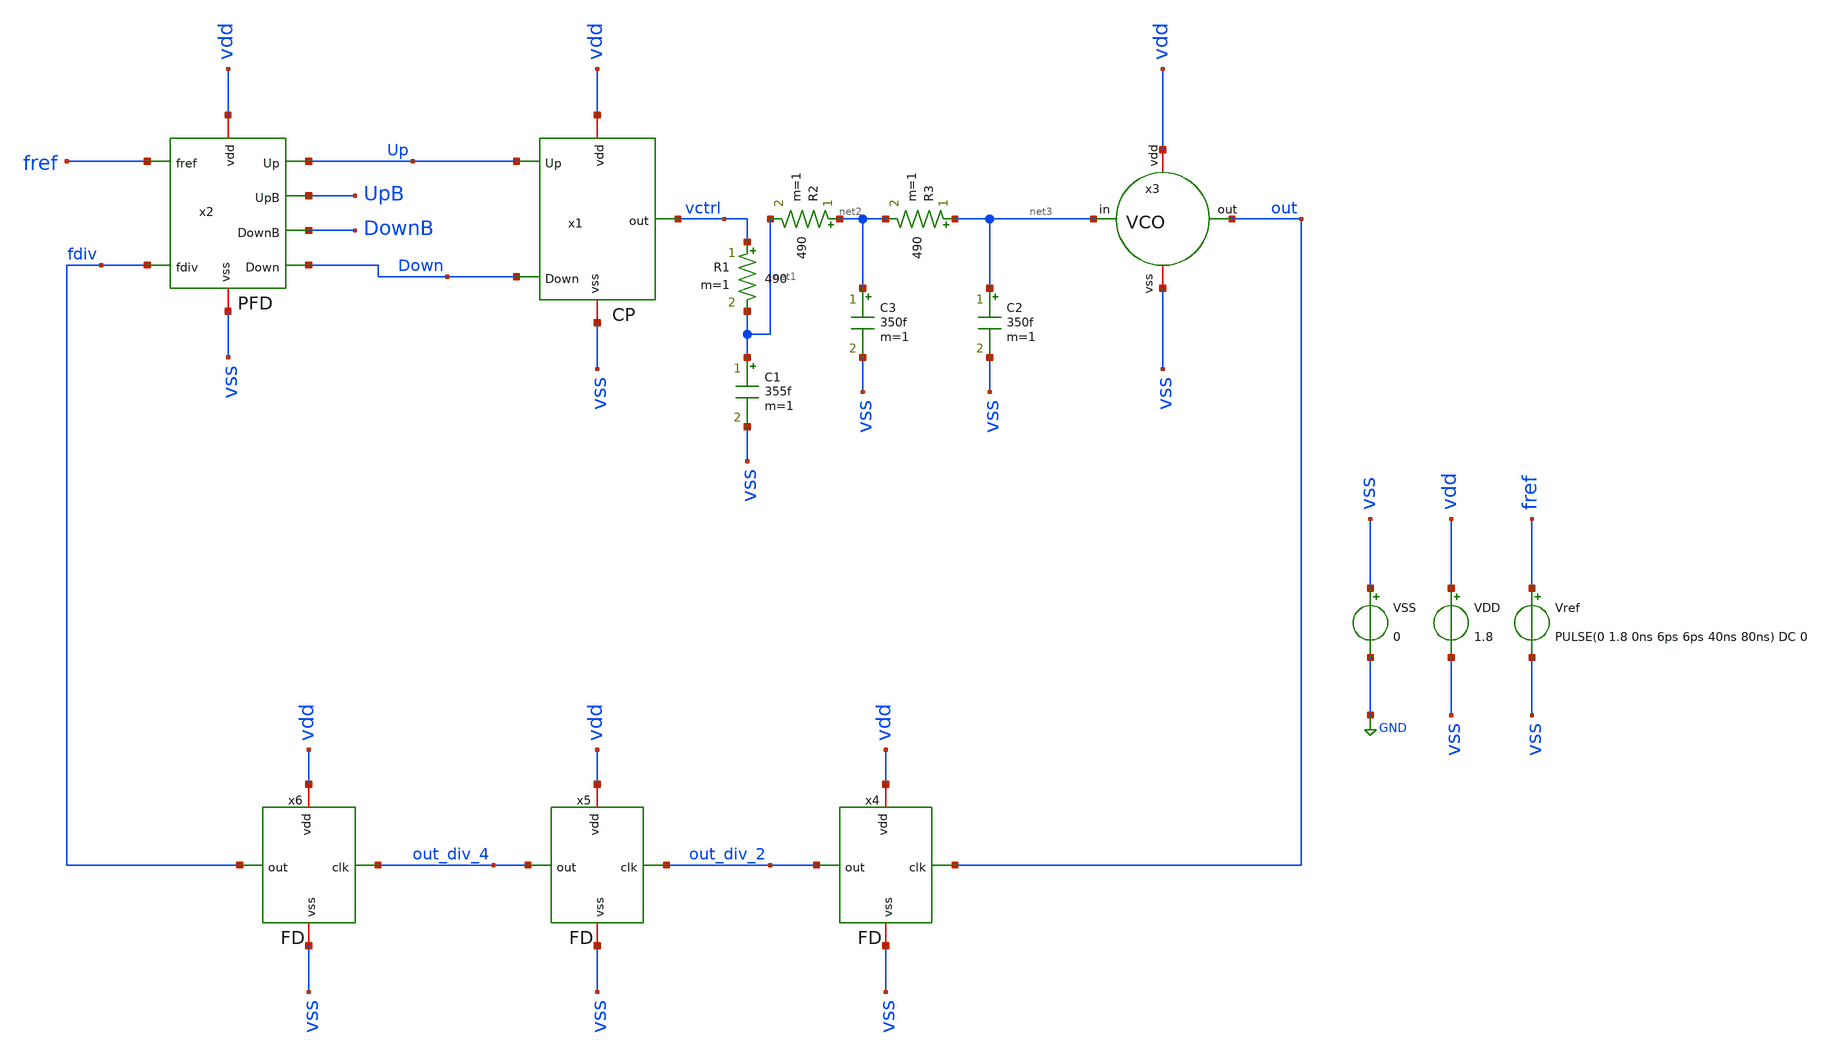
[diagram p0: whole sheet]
** sch_path: sch/PLL_caravel/PLL.sch
**.subckt PLL
x1 vdd Down vctrl Up vss CP
x2 vdd fref Up UpB DownB fdiv Down vss PFD
x3 vdd out net3 vss VCO
x4 out out_div_2 vdd vss FD
C1 net1 vss 355f m=1
R1 vctrl net1 490 m=1
R2 net2 net1 490 m=1
C3 net2 vss 350f m=1
R3 net3 net2 490 m=1
C2 net3 vss 350f m=1
x5 out_div_2 out_div_4 vdd vss FD
x6 out_div_4 fdiv vdd vss FD
VSS vss GND 0
VDD vdd vss 1.8
Vref fref vss PULSE(0 1.8 0ns 6ps 6ps 40ns 80ns) DC 0
**** begin user architecture code



* Parameters
.options TEMPS = 27.0

* Models
.lib ~/skywater/skywater-pdk/libraries/sky130_fd_pr_ngspice/latest/models/corners/sky130.lib TT

* Data to save
.save all

* Simulation
.ic v(vctrl) = 0
.ic v(out_div_2) = 0
.ic v(out_div_4) = 1.8
.ic v(fdiv) = 0
.control
	tran 0.1ns 50us
	plot v(fref)+18 v(fdiv)+18 v(out_div_4)+15 v(out_div_2)+12 v(out)+9 v(up)+6 v(down)+3 v(vctrl)
.endc

.end


**** end user architecture code
**.ends

* expanding   symbol:  PLL_caravel/CP.sym # of pins=5
** sym_path: sch/PLL_caravel/CP.sym
** sch_path: sch/PLL_caravel/CP.sch
.subckt CP vdd Down out Up vss
*.iopin vdd
*.ipin Down
*.opin out
*.iopin vss
*.ipin Up
XM1 outP net1 vdd vdd sky130_fd_pr__pfet_01v8 L=0.15 W=5.4 nf=1 ad='int((nf+1)/2) * W/nf * 0.29' as='int((nf+2)/2) * W/nf * 0.29'
+ pd='2*int((nf+1)/2) * (W/nf + 0.29)' ps='2*int((nf+2)/2) * (W/nf + 0.29)' nrd='0.29 / W' nrs='0.29 / W'
+ sa=0 sb=0 sd=0 mult=1 m=1
XM2 out Up outN vss sky130_fd_pr__nfet_01v8 L=0.15 W=0.42 nf=1 ad='int((nf+1)/2) * W/nf * 0.29' as='int((nf+2)/2) * W/nf * 0.29'
+ pd='2*int((nf+1)/2) * (W/nf + 0.29)' ps='2*int((nf+2)/2) * (W/nf + 0.29)' nrd='0.29 / W' nrs='0.29 / W'
+ sa=0 sb=0 sd=0 mult=1 m=1
XM3 net1 net1 vdd vdd sky130_fd_pr__pfet_01v8 L=0.15 W=0.42 nf=1 ad='int((nf+1)/2) * W/nf * 0.29' as='int((nf+2)/2) * W/nf * 0.29'
+ pd='2*int((nf+1)/2) * (W/nf + 0.29)' ps='2*int((nf+2)/2) * (W/nf + 0.29)' nrd='0.29 / W' nrs='0.29 / W'
+ sa=0 sb=0 sd=0 mult=1 m=1
XM4 out DownB outP vdd sky130_fd_pr__pfet_01v8 L=0.15 W=0.42 nf=1 ad='int((nf+1)/2) * W/nf * 0.29' as='int((nf+2)/2) * W/nf * 0.29'
+ pd='2*int((nf+1)/2) * (W/nf + 0.29)' ps='2*int((nf+2)/2) * (W/nf + 0.29)' nrd='0.29 / W' nrs='0.29 / W'
+ sa=0 sb=0 sd=0 mult=1 m=1
XM5 outN net2 vss vss sky130_fd_pr__nfet_01v8 L=0.15 W=5.4 nf=1 ad='int((nf+1)/2) * W/nf * 0.29' as='int((nf+2)/2) * W/nf * 0.29'
+ pd='2*int((nf+1)/2) * (W/nf + 0.29)' ps='2*int((nf+2)/2) * (W/nf + 0.29)' nrd='0.29 / W' nrs='0.29 / W'
+ sa=0 sb=0 sd=0 mult=1 m=1
XM6 net2 net2 vss vss sky130_fd_pr__nfet_01v8 L=0.15 W=0.42 nf=1 ad='int((nf+1)/2) * W/nf * 0.29' as='int((nf+2)/2) * W/nf * 0.29'
+ pd='2*int((nf+1)/2) * (W/nf + 0.29)' ps='2*int((nf+2)/2) * (W/nf + 0.29)' nrd='0.29 / W' nrs='0.29 / W'
+ sa=0 sb=0 sd=0 mult=1 m=1
XM7 net3 Down outP vdd sky130_fd_pr__pfet_01v8 L=0.15 W=5.4 nf=1 ad='int((nf+1)/2) * W/nf * 0.29' as='int((nf+2)/2) * W/nf * 0.29'
+ pd='2*int((nf+1)/2) * (W/nf + 0.29)' ps='2*int((nf+2)/2) * (W/nf + 0.29)' nrd='0.29 / W' nrs='0.29 / W'
+ sa=0 sb=0 sd=0 mult=1 m=1
XM8 net3 net3 vss vss sky130_fd_pr__nfet_01v8 L=0.15 W=0.42 nf=1 ad='int((nf+1)/2) * W/nf * 0.29' as='int((nf+2)/2) * W/nf * 0.29'
+ pd='2*int((nf+1)/2) * (W/nf + 0.29)' ps='2*int((nf+2)/2) * (W/nf + 0.29)' nrd='0.29 / W' nrs='0.29 / W'
+ sa=0 sb=0 sd=0 mult=1 m=1
XM9 net4 UpB outN vss sky130_fd_pr__nfet_01v8 L=0.15 W=5.4 nf=1 ad='int((nf+1)/2) * W/nf * 0.29' as='int((nf+2)/2) * W/nf * 0.29'
+ pd='2*int((nf+1)/2) * (W/nf + 0.29)' ps='2*int((nf+2)/2) * (W/nf + 0.29)' nrd='0.29 / W' nrs='0.29 / W'
+ sa=0 sb=0 sd=0 mult=1 m=1
XM10 net4 net4 vdd vdd sky130_fd_pr__pfet_01v8 L=0.15 W=0.42 nf=1 ad='int((nf+1)/2) * W/nf * 0.29' as='int((nf+2)/2) * W/nf * 0.29'
+ pd='2*int((nf+1)/2) * (W/nf + 0.29)' ps='2*int((nf+2)/2) * (W/nf + 0.29)' nrd='0.29 / W' nrs='0.29 / W'
+ sa=0 sb=0 sd=0 mult=1 m=1
XM11 DownB Down vdd vdd sky130_fd_pr__pfet_01v8 L=0.15 W=0.84 nf=1 ad='int((nf+1)/2) * W/nf * 0.29' as='int((nf+2)/2) * W/nf * 0.29'
+ pd='2*int((nf+1)/2) * (W/nf + 0.29)' ps='2*int((nf+2)/2) * (W/nf + 0.29)' nrd='0.29 / W' nrs='0.29 / W'
+ sa=0 sb=0 sd=0 mult=1 m=1
XM12 DownB Down vss vss sky130_fd_pr__nfet_01v8 L=0.15 W=0.42 nf=1 ad='int((nf+1)/2) * W/nf * 0.29' as='int((nf+2)/2) * W/nf * 0.29'
+ pd='2*int((nf+1)/2) * (W/nf + 0.29)' ps='2*int((nf+2)/2) * (W/nf + 0.29)' nrd='0.29 / W' nrs='0.29 / W'
+ sa=0 sb=0 sd=0 mult=1 m=1
XM13 UpB Up vdd vdd sky130_fd_pr__pfet_01v8 L=0.15 W=0.84 nf=1 ad='int((nf+1)/2) * W/nf * 0.29' as='int((nf+2)/2) * W/nf * 0.29'
+ pd='2*int((nf+1)/2) * (W/nf + 0.29)' ps='2*int((nf+2)/2) * (W/nf + 0.29)' nrd='0.29 / W' nrs='0.29 / W'
+ sa=0 sb=0 sd=0 mult=1 m=1
XM14 UpB Up vss vss sky130_fd_pr__nfet_01v8 L=0.15 W=0.42 nf=1 ad='int((nf+1)/2) * W/nf * 0.29' as='int((nf+2)/2) * W/nf * 0.29'
+ pd='2*int((nf+1)/2) * (W/nf + 0.29)' ps='2*int((nf+2)/2) * (W/nf + 0.29)' nrd='0.29 / W' nrs='0.29 / W'
+ sa=0 sb=0 sd=0 mult=1 m=1
.ends


* expanding   symbol:  PLL_caravel/PFD.sym # of pins=8
** sym_path: sch/PLL_caravel/PFD.sym
** sch_path: sch/PLL_caravel/PFD.sch
.subckt PFD vdd fref Up UpB DownB fdiv Down vss
*.ipin fref
*.iopin vdd
*.opin Down
*.ipin fdiv
*.iopin vss
*.opin Up
*.opin UpB
*.opin DownB
XM1 out1 fref vdd vdd sky130_fd_pr__pfet_01v8 L=0.15 W={wm1} nf=1 ad='int((nf+1)/2) * W/nf * 0.29' as='int((nf+2)/2) * W/nf * 0.29'
+ pd='2*int((nf+1)/2) * (W/nf + 0.29)' ps='2*int((nf+2)/2) * (W/nf + 0.29)' nrd='0.29 / W' nrs='0.29 / W'
+ sa=0 sb=0 sd=0 mult=1 m=1
XM2 out1 fref net1 vss sky130_fd_pr__nfet_01v8 L=0.15 W=1.8 nf=1 ad='int((nf+1)/2) * W/nf * 0.29' as='int((nf+2)/2) * W/nf * 0.29'
+ pd='2*int((nf+1)/2) * (W/nf + 0.29)' ps='2*int((nf+2)/2) * (W/nf + 0.29)' nrd='0.29 / W' nrs='0.29 / W'
+ sa=0 sb=0 sd=0 mult=1 m=1
XM3 net1 fdiv vss vss sky130_fd_pr__nfet_01v8 L=0.15 W=0.42 nf=1 ad='int((nf+1)/2) * W/nf * 0.29' as='int((nf+2)/2) * W/nf * 0.29'
+ pd='2*int((nf+1)/2) * (W/nf + 0.29)' ps='2*int((nf+2)/2) * (W/nf + 0.29)' nrd='0.29 / W' nrs='0.29 / W'
+ sa=0 sb=0 sd=0 mult=1 m=1
XM4 out2 fdiv vdd vdd sky130_fd_pr__pfet_01v8 L=0.15 W=0.64 nf=1 ad='int((nf+1)/2) * W/nf * 0.29' as='int((nf+2)/2) * W/nf * 0.29'
+ pd='2*int((nf+1)/2) * (W/nf + 0.29)' ps='2*int((nf+2)/2) * (W/nf + 0.29)' nrd='0.29 / W' nrs='0.29 / W'
+ sa=0 sb=0 sd=0 mult=1 m=1
XM5 out2 fdiv net2 vss sky130_fd_pr__nfet_01v8 L=0.15 W=1.8 nf=1 ad='int((nf+1)/2) * W/nf * 0.29' as='int((nf+2)/2) * W/nf * 0.29'
+ pd='2*int((nf+1)/2) * (W/nf + 0.29)' ps='2*int((nf+2)/2) * (W/nf + 0.29)' nrd='0.29 / W' nrs='0.29 / W'
+ sa=0 sb=0 sd=0 mult=1 m=1
XM6 net2 fref vss vss sky130_fd_pr__nfet_01v8 L=0.15 W=0.42 nf=1 ad='int((nf+1)/2) * W/nf * 0.29' as='int((nf+2)/2) * W/nf * 0.29'
+ pd='2*int((nf+1)/2) * (W/nf + 0.29)' ps='2*int((nf+2)/2) * (W/nf + 0.29)' nrd='0.29 / W' nrs='0.29 / W'
+ sa=0 sb=0 sd=0 mult=1 m=1
XM7 out3 fref fref vdd sky130_fd_pr__pfet_01v8 L=0.15 W=0.64 nf=1 ad='int((nf+1)/2) * W/nf * 0.29' as='int((nf+2)/2) * W/nf * 0.29'
+ pd='2*int((nf+1)/2) * (W/nf + 0.29)' ps='2*int((nf+2)/2) * (W/nf + 0.29)' nrd='0.29 / W' nrs='0.29 / W'
+ sa=0 sb=0 sd=0 mult=1 m=1
XM8 out3 fref out1 vss sky130_fd_pr__nfet_01v8 L=0.15 W=0.84 nf=1 ad='int((nf+1)/2) * W/nf * 0.29' as='int((nf+2)/2) * W/nf * 0.29'
+ pd='2*int((nf+1)/2) * (W/nf + 0.29)' ps='2*int((nf+2)/2) * (W/nf + 0.29)' nrd='0.29 / W' nrs='0.29 / W'
+ sa=0 sb=0 sd=0 mult=1 m=1
XM9 out4 fdiv fdiv vdd sky130_fd_pr__pfet_01v8 L=0.15 W=0.64 nf=1 ad='int((nf+1)/2) * W/nf * 0.29' as='int((nf+2)/2) * W/nf * 0.29'
+ pd='2*int((nf+1)/2) * (W/nf + 0.29)' ps='2*int((nf+2)/2) * (W/nf + 0.29)' nrd='0.29 / W' nrs='0.29 / W'
+ sa=0 sb=0 sd=0 mult=1 m=1
XM10 out4 fdiv out2 vss sky130_fd_pr__nfet_01v8 L=0.15 W=0.84 nf=1 ad='int((nf+1)/2) * W/nf * 0.29' as='int((nf+2)/2) * W/nf * 0.29'
+ pd='2*int((nf+1)/2) * (W/nf + 0.29)' ps='2*int((nf+2)/2) * (W/nf + 0.29)' nrd='0.29 / W' nrs='0.29 / W'
+ sa=0 sb=0 sd=0 mult=1 m=1
XM11 UpB out3 vdd vdd sky130_fd_pr__pfet_01v8 L=0.15 W=0.84 nf=1 ad='int((nf+1)/2) * W/nf * 0.29' as='int((nf+2)/2) * W/nf * 0.29'
+ pd='2*int((nf+1)/2) * (W/nf + 0.29)' ps='2*int((nf+2)/2) * (W/nf + 0.29)' nrd='0.29 / W' nrs='0.29 / W'
+ sa=0 sb=0 sd=0 mult=1 m=1
XM12 UpB out3 vss vss sky130_fd_pr__nfet_01v8 L=0.15 W=0.42 nf=1 ad='int((nf+1)/2) * W/nf * 0.29' as='int((nf+2)/2) * W/nf * 0.29'
+ pd='2*int((nf+1)/2) * (W/nf + 0.29)' ps='2*int((nf+2)/2) * (W/nf + 0.29)' nrd='0.29 / W' nrs='0.29 / W'
+ sa=0 sb=0 sd=0 mult=1 m=1
XM13 Up UpB vdd vdd sky130_fd_pr__pfet_01v8 L=0.15 W=0.96 nf=1 ad='int((nf+1)/2) * W/nf * 0.29' as='int((nf+2)/2) * W/nf * 0.29'
+ pd='2*int((nf+1)/2) * (W/nf + 0.29)' ps='2*int((nf+2)/2) * (W/nf + 0.29)' nrd='0.29 / W' nrs='0.29 / W'
+ sa=0 sb=0 sd=0 mult=1 m=1
XM14 Up UpB vss vss sky130_fd_pr__nfet_01v8 L=0.15 W=0.64 nf=1 ad='int((nf+1)/2) * W/nf * 0.29' as='int((nf+2)/2) * W/nf * 0.29'
+ pd='2*int((nf+1)/2) * (W/nf + 0.29)' ps='2*int((nf+2)/2) * (W/nf + 0.29)' nrd='0.29 / W' nrs='0.29 / W'
+ sa=0 sb=0 sd=0 mult=1 m=1
XM15 DownB out4 vdd vdd sky130_fd_pr__pfet_01v8 L=0.15 W=0.84 nf=1 ad='int((nf+1)/2) * W/nf * 0.29' as='int((nf+2)/2) * W/nf * 0.29'
+ pd='2*int((nf+1)/2) * (W/nf + 0.29)' ps='2*int((nf+2)/2) * (W/nf + 0.29)' nrd='0.29 / W' nrs='0.29 / W'
+ sa=0 sb=0 sd=0 mult=1 m=1
XM16 DownB out4 vss vss sky130_fd_pr__nfet_01v8 L=0.15 W=0.42 nf=1 ad='int((nf+1)/2) * W/nf * 0.29' as='int((nf+2)/2) * W/nf * 0.29'
+ pd='2*int((nf+1)/2) * (W/nf + 0.29)' ps='2*int((nf+2)/2) * (W/nf + 0.29)' nrd='0.29 / W' nrs='0.29 / W'
+ sa=0 sb=0 sd=0 mult=1 m=1
XM17 Down DownB vdd vdd sky130_fd_pr__pfet_01v8 L=0.15 W=0.96 nf=1 ad='int((nf+1)/2) * W/nf * 0.29' as='int((nf+2)/2) * W/nf * 0.29'
+ pd='2*int((nf+1)/2) * (W/nf + 0.29)' ps='2*int((nf+2)/2) * (W/nf + 0.29)' nrd='0.29 / W' nrs='0.29 / W'
+ sa=0 sb=0 sd=0 mult=1 m=1
XM18 Down DownB vss vss sky130_fd_pr__nfet_01v8 L=0.15 W=0.64 nf=1 ad='int((nf+1)/2) * W/nf * 0.29' as='int((nf+2)/2) * W/nf * 0.29'
+ pd='2*int((nf+1)/2) * (W/nf + 0.29)' ps='2*int((nf+2)/2) * (W/nf + 0.29)' nrd='0.29 / W' nrs='0.29 / W'
+ sa=0 sb=0 sd=0 mult=1 m=1
.ends


* expanding   symbol:  PLL_caravel/VCO.sym # of pins=4
** sym_path: sch/PLL_caravel/VCO.sym
** sch_path: sch/PLL_caravel/VCO.sch
.subckt VCO vdd out in vss
*.iopin vdd
*.iopin vss
*.ipin in
*.opin out
x1 vdd_ro ring_out o1 vss_ro NOT
x2 vdd_ro o1 o2 vss_ro NOT
x3 vdd_ro o2 o3 vss_ro NOT
x4 vdd_ro o3 o4 vss_ro NOT
x5 vdd_ro o4 o5 vss_ro NOT
x6 vdd_ro o5 o6 vss_ro NOT
XM1 vdd_ro pol vdd vdd sky130_fd_pr__pfet_01v8 L=0.15 W=1.08 nf=1 ad='int((nf+1)/2) * W/nf * 0.29' as='int((nf+2)/2) * W/nf * 0.29'
+ pd='2*int((nf+1)/2) * (W/nf + 0.29)' ps='2*int((nf+2)/2) * (W/nf + 0.29)' nrd='0.29 / W' nrs='0.29 / W'
+ sa=0 sb=0 sd=0 mult=1 m=1
XM2 vss_ro in vss vss sky130_fd_pr__nfet_01v8 L=0.15 W=1.08 nf=1 ad='int((nf+1)/2) * W/nf * 0.29' as='int((nf+2)/2) * W/nf * 0.29'
+ pd='2*int((nf+1)/2) * (W/nf + 0.29)' ps='2*int((nf+2)/2) * (W/nf + 0.29)' nrd='0.29 / W' nrs='0.29 / W'
+ sa=0 sb=0 sd=0 mult=1 m=1
XM3 pol pol vdd vdd sky130_fd_pr__pfet_01v8 L=0.15 W=0.84 nf=1 ad='int((nf+1)/2) * W/nf * 0.29' as='int((nf+2)/2) * W/nf * 0.29'
+ pd='2*int((nf+1)/2) * (W/nf + 0.29)' ps='2*int((nf+2)/2) * (W/nf + 0.29)' nrd='0.29 / W' nrs='0.29 / W'
+ sa=0 sb=0 sd=0 mult=1 m=1
XM4 vss in pol vss sky130_fd_pr__nfet_01v8 L=0.15 W=0.84 nf=1 ad='int((nf+1)/2) * W/nf * 0.29' as='int((nf+2)/2) * W/nf * 0.29'
+ pd='2*int((nf+1)/2) * (W/nf + 0.29)' ps='2*int((nf+2)/2) * (W/nf + 0.29)' nrd='0.29 / W' nrs='0.29 / W'
+ sa=0 sb=0 sd=0 mult=1 m=1
XM5 out ring_out vdd vdd sky130_fd_pr__pfet_01v8 L=0.15 W=1.08 nf=1 ad='int((nf+1)/2) * W/nf * 0.29'
+ as='int((nf+2)/2) * W/nf * 0.29' pd='2*int((nf+1)/2) * (W/nf + 0.29)' ps='2*int((nf+2)/2) * (W/nf + 0.29)'
+ nrd='0.29 / W' nrs='0.29 / W' sa=0 sb=0 sd=0 mult=1 m=1
XM6 out ring_out vss vss sky130_fd_pr__nfet_01v8 L=0.15 W=0.54 nf=1 ad='int((nf+1)/2) * W/nf * 0.29'
+ as='int((nf+2)/2) * W/nf * 0.29' pd='2*int((nf+1)/2) * (W/nf + 0.29)' ps='2*int((nf+2)/2) * (W/nf + 0.29)'
+ nrd='0.29 / W' nrs='0.29 / W' sa=0 sb=0 sd=0 mult=1 m=1
XM7 ring_out o6 vdd_ro vdd_ro sky130_fd_pr__pfet_01v8 L=0.15 W=2.4 nf=1 ad='int((nf+1)/2) * W/nf * 0.29'
+ as='int((nf+2)/2) * W/nf * 0.29' pd='2*int((nf+1)/2) * (W/nf + 0.29)' ps='2*int((nf+2)/2) * (W/nf + 0.29)'
+ nrd='0.29 / W' nrs='0.29 / W' sa=0 sb=0 sd=0 mult=1 m=1
XM8 ring_out o6 vss_ro vss_ro sky130_fd_pr__nfet_01v8 L=0.15 W=1.2 nf=1 ad='int((nf+1)/2) * W/nf * 0.29'
+ as='int((nf+2)/2) * W/nf * 0.29' pd='2*int((nf+1)/2) * (W/nf + 0.29)' ps='2*int((nf+2)/2) * (W/nf + 0.29)'
+ nrd='0.29 / W' nrs='0.29 / W' sa=0 sb=0 sd=0 mult=1 m=1
.ends


* expanding   symbol:  PLL_caravel/FD.sym # of pins=4
** sym_path: sch/PLL_caravel/FD.sym
** sch_path: sch/PLL_caravel/FD.sch
.subckt FD clk out vdd vss
*.iopin vss
*.ipin clk
*.opin out
*.iopin vdd
XM1 net1 out1 vdd vdd sky130_fd_pr__pfet_01v8 L=0.15 W=0.84 nf=1 ad='int((nf+1)/2) * W/nf * 0.29' as='int((nf+2)/2) * W/nf * 0.29'
+ pd='2*int((nf+1)/2) * (W/nf + 0.29)' ps='2*int((nf+2)/2) * (W/nf + 0.29)' nrd='0.29 / W' nrs='0.29 / W'
+ sa=0 sb=0 sd=0 mult=1 m=1
XM2 net1 out1 vss vss sky130_fd_pr__nfet_01v8 L=0.15 W=0.42 nf=1 ad='int((nf+1)/2) * W/nf * 0.29' as='int((nf+2)/2) * W/nf * 0.29'
+ pd='2*int((nf+1)/2) * (W/nf + 0.29)' ps='2*int((nf+2)/2) * (W/nf + 0.29)' nrd='0.29 / W' nrs='0.29 / W'
+ sa=0 sb=0 sd=0 mult=1 m=1
XM3 net1 clkb net2 vdd sky130_fd_pr__pfet_01v8 L=0.15 W=0.84 nf=1 ad='int((nf+1)/2) * W/nf * 0.29' as='int((nf+2)/2) * W/nf * 0.29'
+ pd='2*int((nf+1)/2) * (W/nf + 0.29)' ps='2*int((nf+2)/2) * (W/nf + 0.29)' nrd='0.29 / W' nrs='0.29 / W'
+ sa=0 sb=0 sd=0 mult=1 m=1
XM4 net1 clk net2 vss sky130_fd_pr__nfet_01v8 L=0.15 W=0.42 nf=1 ad='int((nf+1)/2) * W/nf * 0.29' as='int((nf+2)/2) * W/nf * 0.29'
+ pd='2*int((nf+1)/2) * (W/nf + 0.29)' ps='2*int((nf+2)/2) * (W/nf + 0.29)' nrd='0.29 / W' nrs='0.29 / W'
+ sa=0 sb=0 sd=0 mult=1 m=1
XM5 net3 net2 vdd vdd sky130_fd_pr__pfet_01v8 L=0.15 W=0.84 nf=1 ad='int((nf+1)/2) * W/nf * 0.29' as='int((nf+2)/2) * W/nf * 0.29'
+ pd='2*int((nf+1)/2) * (W/nf + 0.29)' ps='2*int((nf+2)/2) * (W/nf + 0.29)' nrd='0.29 / W' nrs='0.29 / W'
+ sa=0 sb=0 sd=0 mult=1 m=1
XM6 net3 net2 vss vss sky130_fd_pr__nfet_01v8 L=0.15 W=0.42 nf=1 ad='int((nf+1)/2) * W/nf * 0.29' as='int((nf+2)/2) * W/nf * 0.29'
+ pd='2*int((nf+1)/2) * (W/nf + 0.29)' ps='2*int((nf+2)/2) * (W/nf + 0.29)' nrd='0.29 / W' nrs='0.29 / W'
+ sa=0 sb=0 sd=0 mult=1 m=1
XM7 net3 clk out vdd sky130_fd_pr__pfet_01v8 L=0.15 W=0.84 nf=1 ad='int((nf+1)/2) * W/nf * 0.29' as='int((nf+2)/2) * W/nf * 0.29'
+ pd='2*int((nf+1)/2) * (W/nf + 0.29)' ps='2*int((nf+2)/2) * (W/nf + 0.29)' nrd='0.29 / W' nrs='0.29 / W'
+ sa=0 sb=0 sd=0 mult=1 m=1
XM8 net3 clkb out vss sky130_fd_pr__nfet_01v8 L=0.15 W=0.42 nf=1 ad='int((nf+1)/2) * W/nf * 0.29' as='int((nf+2)/2) * W/nf * 0.29'
+ pd='2*int((nf+1)/2) * (W/nf + 0.29)' ps='2*int((nf+2)/2) * (W/nf + 0.29)' nrd='0.29 / W' nrs='0.29 / W'
+ sa=0 sb=0 sd=0 mult=1 m=1
XM9 out1 out vdd vdd sky130_fd_pr__pfet_01v8 L=0.15 W=0.84 nf=1 ad='int((nf+1)/2) * W/nf * 0.29' as='int((nf+2)/2) * W/nf * 0.29'
+ pd='2*int((nf+1)/2) * (W/nf + 0.29)' ps='2*int((nf+2)/2) * (W/nf + 0.29)' nrd='0.29 / W' nrs='0.29 / W'
+ sa=0 sb=0 sd=0 mult=1 m=1
XM10 out1 out vss vss sky130_fd_pr__nfet_01v8 L=0.15 W=0.42 nf=1 ad='int((nf+1)/2) * W/nf * 0.29' as='int((nf+2)/2) * W/nf * 0.29'
+ pd='2*int((nf+1)/2) * (W/nf + 0.29)' ps='2*int((nf+2)/2) * (W/nf + 0.29)' nrd='0.29 / W' nrs='0.29 / W'
+ sa=0 sb=0 sd=0 mult=1 m=1
XM11 clkb clk vdd vdd sky130_fd_pr__pfet_01v8 L=0.15 W=0.84 nf=1 ad='int((nf+1)/2) * W/nf * 0.29' as='int((nf+2)/2) * W/nf * 0.29'
+ pd='2*int((nf+1)/2) * (W/nf + 0.29)' ps='2*int((nf+2)/2) * (W/nf + 0.29)' nrd='0.29 / W' nrs='0.29 / W'
+ sa=0 sb=0 sd=0 mult=1 m=1
XM12 clkb clk vss vss sky130_fd_pr__nfet_01v8 L=0.15 W=0.42 nf=1 ad='int((nf+1)/2) * W/nf * 0.29' as='int((nf+2)/2) * W/nf * 0.29'
+ pd='2*int((nf+1)/2) * (W/nf + 0.29)' ps='2*int((nf+2)/2) * (W/nf + 0.29)' nrd='0.29 / W' nrs='0.29 / W'
+ sa=0 sb=0 sd=0 mult=1 m=1
.ends


* expanding   symbol:  PLL_caravel/NOT.sym # of pins=4
** sym_path: sch/PLL_caravel/NOT.sym
** sch_path: sch/PLL_caravel/NOT.sch
.subckt NOT vdd in out vss
*.iopin vdd
*.iopin vss
*.ipin in
*.opin out
XM1 out in vdd vdd sky130_fd_pr__pfet_01v8 L=0.15 W=0.84 nf=1 ad='int((nf+1)/2) * W/nf * 0.29' as='int((nf+2)/2) * W/nf * 0.29'
+ pd='2*int((nf+1)/2) * (W/nf + 0.29)' ps='2*int((nf+2)/2) * (W/nf + 0.29)' nrd='0.29 / W' nrs='0.29 / W'
+ sa=0 sb=0 sd=0 mult=1 m=1
XM2 out in vss vss sky130_fd_pr__nfet_01v8 L=0.15 W=0.42 nf=1 ad='int((nf+1)/2) * W/nf * 0.29' as='int((nf+2)/2) * W/nf * 0.29'
+ pd='2*int((nf+1)/2) * (W/nf + 0.29)' ps='2*int((nf+2)/2) * (W/nf + 0.29)' nrd='0.29 / W' nrs='0.29 / W'
+ sa=0 sb=0 sd=0 mult=1 m=1
.ends

.GLOBAL GND
.end
